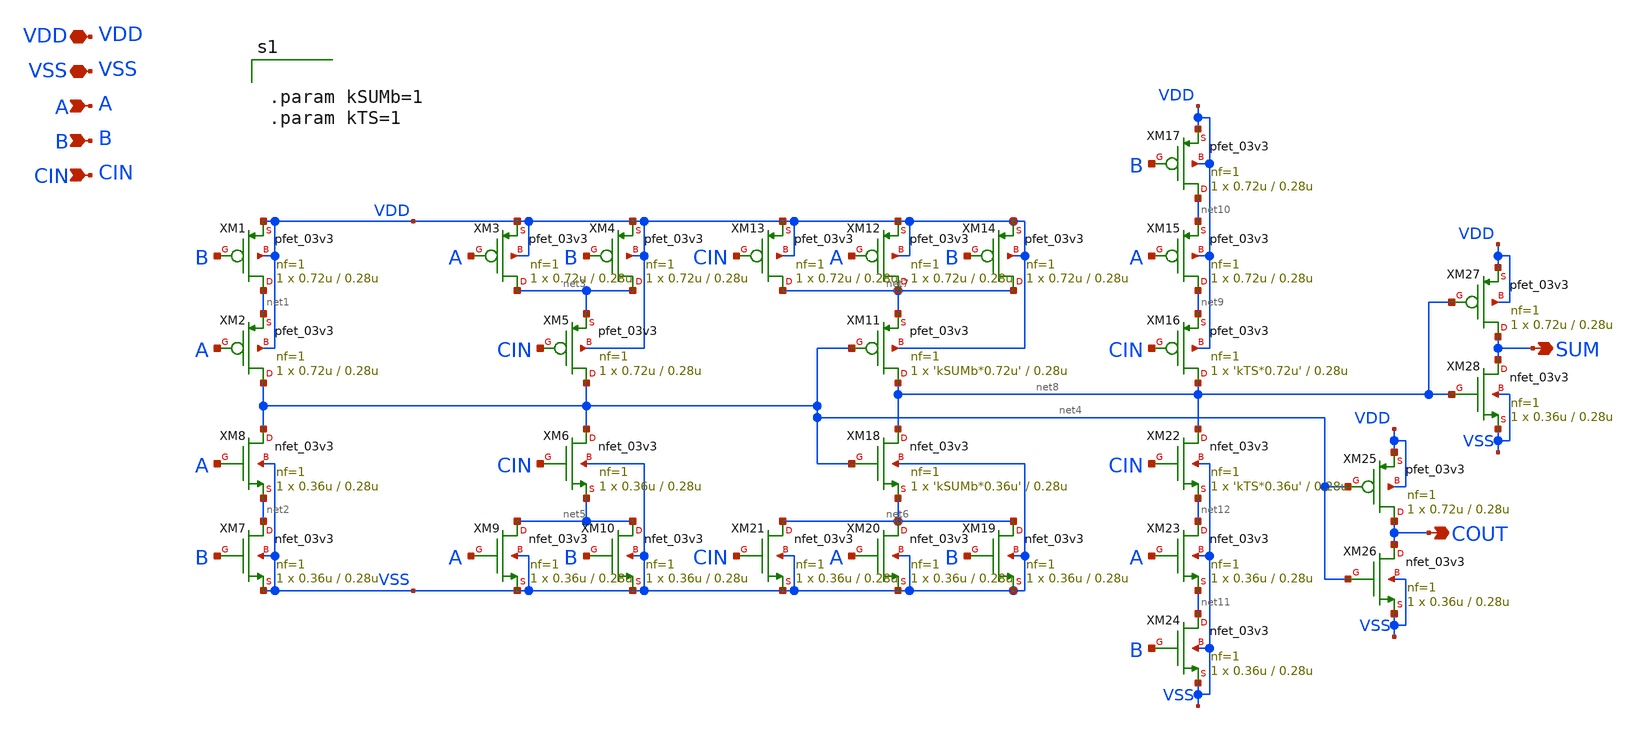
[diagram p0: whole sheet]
** sch_path: CAD6/pc_full_adder.sch
**.subckt pc_full_adder VDD VSS A B CIN COUT SUM
*.iopin VDD
*.iopin VSS
*.ipin A
*.ipin B
*.ipin CIN
*.opin COUT
*.opin SUM
XM1 net1 B VDD VDD pfet_03v3 L=0.28u W=0.72u nf=1 ad='int((nf+1)/2) * W/nf * 0.18u' as='int((nf+2)/2) * W/nf * 0.18u'
+ pd='2*int((nf+1)/2) * (W/nf + 0.18u)' ps='2*int((nf+2)/2) * (W/nf + 0.18u)' nrd='0.18u / W' nrs='0.18u / W'
+ sa=0 sb=0 sd=0 m=1
XM2 net4 A net1 VDD pfet_03v3 L=0.28u W=0.72u nf=1 ad='int((nf+1)/2) * W/nf * 0.18u' as='int((nf+2)/2) * W/nf * 0.18u'
+ pd='2*int((nf+1)/2) * (W/nf + 0.18u)' ps='2*int((nf+2)/2) * (W/nf + 0.18u)' nrd='0.18u / W' nrs='0.18u / W'
+ sa=0 sb=0 sd=0 m=1
XM3 net3 A VDD VDD pfet_03v3 L=0.28u W=0.72u nf=1 ad='int((nf+1)/2) * W/nf * 0.18u' as='int((nf+2)/2) * W/nf * 0.18u'
+ pd='2*int((nf+1)/2) * (W/nf + 0.18u)' ps='2*int((nf+2)/2) * (W/nf + 0.18u)' nrd='0.18u / W' nrs='0.18u / W'
+ sa=0 sb=0 sd=0 m=1
XM4 net3 B VDD VDD pfet_03v3 L=0.28u W=0.72u nf=1 ad='int((nf+1)/2) * W/nf * 0.18u' as='int((nf+2)/2) * W/nf * 0.18u'
+ pd='2*int((nf+1)/2) * (W/nf + 0.18u)' ps='2*int((nf+2)/2) * (W/nf + 0.18u)' nrd='0.18u / W' nrs='0.18u / W'
+ sa=0 sb=0 sd=0 m=1
XM5 net4 CIN net3 VDD pfet_03v3 L=0.28u W=0.72u nf=1 ad='int((nf+1)/2) * W/nf * 0.18u' as='int((nf+2)/2) * W/nf * 0.18u'
+ pd='2*int((nf+1)/2) * (W/nf + 0.18u)' ps='2*int((nf+2)/2) * (W/nf + 0.18u)' nrd='0.18u / W' nrs='0.18u / W'
+ sa=0 sb=0 sd=0 m=1
XM6 net4 CIN net5 VSS nfet_03v3 L=0.28u W=0.36u nf=1 ad='int((nf+1)/2) * W/nf * 0.18u' as='int((nf+2)/2) * W/nf * 0.18u'
+ pd='2*int((nf+1)/2) * (W/nf + 0.18u)' ps='2*int((nf+2)/2) * (W/nf + 0.18u)' nrd='0.18u / W' nrs='0.18u / W'
+ sa=0 sb=0 sd=0 m=1
XM7 net2 B VSS VSS nfet_03v3 L=0.28u W=0.36u nf=1 ad='int((nf+1)/2) * W/nf * 0.18u' as='int((nf+2)/2) * W/nf * 0.18u'
+ pd='2*int((nf+1)/2) * (W/nf + 0.18u)' ps='2*int((nf+2)/2) * (W/nf + 0.18u)' nrd='0.18u / W' nrs='0.18u / W'
+ sa=0 sb=0 sd=0 m=1
XM8 net4 A net2 VSS nfet_03v3 L=0.28u W=0.36u nf=1 ad='int((nf+1)/2) * W/nf * 0.18u' as='int((nf+2)/2) * W/nf * 0.18u'
+ pd='2*int((nf+1)/2) * (W/nf + 0.18u)' ps='2*int((nf+2)/2) * (W/nf + 0.18u)' nrd='0.18u / W' nrs='0.18u / W'
+ sa=0 sb=0 sd=0 m=1
XM9 net5 A VSS VSS nfet_03v3 L=0.28u W=0.36u nf=1 ad='int((nf+1)/2) * W/nf * 0.18u' as='int((nf+2)/2) * W/nf * 0.18u'
+ pd='2*int((nf+1)/2) * (W/nf + 0.18u)' ps='2*int((nf+2)/2) * (W/nf + 0.18u)' nrd='0.18u / W' nrs='0.18u / W'
+ sa=0 sb=0 sd=0 m=1
XM10 net5 B VSS VSS nfet_03v3 L=0.28u W=0.36u nf=1 ad='int((nf+1)/2) * W/nf * 0.18u' as='int((nf+2)/2) * W/nf * 0.18u'
+ pd='2*int((nf+1)/2) * (W/nf + 0.18u)' ps='2*int((nf+2)/2) * (W/nf + 0.18u)' nrd='0.18u / W' nrs='0.18u / W'
+ sa=0 sb=0 sd=0 m=1
XM11 net8 net4 net7 VDD pfet_03v3 L=0.28u W='kSUMb*0.72u' nf=1 ad='int((nf+1)/2) * W/nf * 0.18u' as='int((nf+2)/2) * W/nf * 0.18u'
+ pd='2*int((nf+1)/2) * (W/nf + 0.18u)' ps='2*int((nf+2)/2) * (W/nf + 0.18u)' nrd='0.18u / W' nrs='0.18u / W'
+ sa=0 sb=0 sd=0 m=1
XM12 net7 A VDD VDD pfet_03v3 L=0.28u W=0.72u nf=1 ad='int((nf+1)/2) * W/nf * 0.18u' as='int((nf+2)/2) * W/nf * 0.18u'
+ pd='2*int((nf+1)/2) * (W/nf + 0.18u)' ps='2*int((nf+2)/2) * (W/nf + 0.18u)' nrd='0.18u / W' nrs='0.18u / W'
+ sa=0 sb=0 sd=0 m=1
XM13 net7 CIN VDD VDD pfet_03v3 L=0.28u W=0.72u nf=1 ad='int((nf+1)/2) * W/nf * 0.18u' as='int((nf+2)/2) * W/nf * 0.18u'
+ pd='2*int((nf+1)/2) * (W/nf + 0.18u)' ps='2*int((nf+2)/2) * (W/nf + 0.18u)' nrd='0.18u / W' nrs='0.18u / W'
+ sa=0 sb=0 sd=0 m=1
XM14 net7 B VDD VDD pfet_03v3 L=0.28u W=0.72u nf=1 ad='int((nf+1)/2) * W/nf * 0.18u' as='int((nf+2)/2) * W/nf * 0.18u'
+ pd='2*int((nf+1)/2) * (W/nf + 0.18u)' ps='2*int((nf+2)/2) * (W/nf + 0.18u)' nrd='0.18u / W' nrs='0.18u / W'
+ sa=0 sb=0 sd=0 m=1
XM15 net9 A net10 VDD pfet_03v3 L=0.28u W=0.72u nf=1 ad='int((nf+1)/2) * W/nf * 0.18u' as='int((nf+2)/2) * W/nf * 0.18u'
+ pd='2*int((nf+1)/2) * (W/nf + 0.18u)' ps='2*int((nf+2)/2) * (W/nf + 0.18u)' nrd='0.18u / W' nrs='0.18u / W'
+ sa=0 sb=0 sd=0 m=1
XM16 net8 CIN net9 VDD pfet_03v3 L=0.28u W='kTS*0.72u' nf=1 ad='int((nf+1)/2) * W/nf * 0.18u' as='int((nf+2)/2) * W/nf * 0.18u'
+ pd='2*int((nf+1)/2) * (W/nf + 0.18u)' ps='2*int((nf+2)/2) * (W/nf + 0.18u)' nrd='0.18u / W' nrs='0.18u / W'
+ sa=0 sb=0 sd=0 m=1
XM17 net10 B VDD VDD pfet_03v3 L=0.28u W=0.72u nf=1 ad='int((nf+1)/2) * W/nf * 0.18u' as='int((nf+2)/2) * W/nf * 0.18u'
+ pd='2*int((nf+1)/2) * (W/nf + 0.18u)' ps='2*int((nf+2)/2) * (W/nf + 0.18u)' nrd='0.18u / W' nrs='0.18u / W'
+ sa=0 sb=0 sd=0 m=1
XM18 net8 net4 net6 VSS nfet_03v3 L=0.28u W='kSUMb*0.36u' nf=1 ad='int((nf+1)/2) * W/nf * 0.18u' as='int((nf+2)/2) * W/nf * 0.18u'
+ pd='2*int((nf+1)/2) * (W/nf + 0.18u)' ps='2*int((nf+2)/2) * (W/nf + 0.18u)' nrd='0.18u / W' nrs='0.18u / W'
+ sa=0 sb=0 sd=0 m=1
XM19 net6 B VSS VSS nfet_03v3 L=0.28u W=0.36u nf=1 ad='int((nf+1)/2) * W/nf * 0.18u' as='int((nf+2)/2) * W/nf * 0.18u'
+ pd='2*int((nf+1)/2) * (W/nf + 0.18u)' ps='2*int((nf+2)/2) * (W/nf + 0.18u)' nrd='0.18u / W' nrs='0.18u / W'
+ sa=0 sb=0 sd=0 m=1
XM20 net6 A VSS VSS nfet_03v3 L=0.28u W=0.36u nf=1 ad='int((nf+1)/2) * W/nf * 0.18u' as='int((nf+2)/2) * W/nf * 0.18u'
+ pd='2*int((nf+1)/2) * (W/nf + 0.18u)' ps='2*int((nf+2)/2) * (W/nf + 0.18u)' nrd='0.18u / W' nrs='0.18u / W'
+ sa=0 sb=0 sd=0 m=1
XM21 net6 CIN VSS VSS nfet_03v3 L=0.28u W=0.36u nf=1 ad='int((nf+1)/2) * W/nf * 0.18u' as='int((nf+2)/2) * W/nf * 0.18u'
+ pd='2*int((nf+1)/2) * (W/nf + 0.18u)' ps='2*int((nf+2)/2) * (W/nf + 0.18u)' nrd='0.18u / W' nrs='0.18u / W'
+ sa=0 sb=0 sd=0 m=1
XM22 net8 CIN net12 VSS nfet_03v3 L=0.28u W='kTS*0.36u' nf=1 ad='int((nf+1)/2) * W/nf * 0.18u' as='int((nf+2)/2) * W/nf * 0.18u'
+ pd='2*int((nf+1)/2) * (W/nf + 0.18u)' ps='2*int((nf+2)/2) * (W/nf + 0.18u)' nrd='0.18u / W' nrs='0.18u / W'
+ sa=0 sb=0 sd=0 m=1
XM23 net12 A net11 VSS nfet_03v3 L=0.28u W=0.36u nf=1 ad='int((nf+1)/2) * W/nf * 0.18u' as='int((nf+2)/2) * W/nf * 0.18u'
+ pd='2*int((nf+1)/2) * (W/nf + 0.18u)' ps='2*int((nf+2)/2) * (W/nf + 0.18u)' nrd='0.18u / W' nrs='0.18u / W'
+ sa=0 sb=0 sd=0 m=1
XM24 net11 B VSS VSS nfet_03v3 L=0.28u W=0.36u nf=1 ad='int((nf+1)/2) * W/nf * 0.18u' as='int((nf+2)/2) * W/nf * 0.18u'
+ pd='2*int((nf+1)/2) * (W/nf + 0.18u)' ps='2*int((nf+2)/2) * (W/nf + 0.18u)' nrd='0.18u / W' nrs='0.18u / W'
+ sa=0 sb=0 sd=0 m=1
XM25 COUT net4 VDD VDD pfet_03v3 L=0.28u W=0.72u nf=1 ad='int((nf+1)/2) * W/nf * 0.18u' as='int((nf+2)/2) * W/nf * 0.18u'
+ pd='2*int((nf+1)/2) * (W/nf + 0.18u)' ps='2*int((nf+2)/2) * (W/nf + 0.18u)' nrd='0.18u / W' nrs='0.18u / W'
+ sa=0 sb=0 sd=0 m=1
XM26 COUT net4 VSS VSS nfet_03v3 L=0.28u W=0.36u nf=1 ad='int((nf+1)/2) * W/nf * 0.18u' as='int((nf+2)/2) * W/nf * 0.18u'
+ pd='2*int((nf+1)/2) * (W/nf + 0.18u)' ps='2*int((nf+2)/2) * (W/nf + 0.18u)' nrd='0.18u / W' nrs='0.18u / W'
+ sa=0 sb=0 sd=0 m=1
XM27 SUM net8 VDD VDD pfet_03v3 L=0.28u W=0.72u nf=1 ad='int((nf+1)/2) * W/nf * 0.18u' as='int((nf+2)/2) * W/nf * 0.18u'
+ pd='2*int((nf+1)/2) * (W/nf + 0.18u)' ps='2*int((nf+2)/2) * (W/nf + 0.18u)' nrd='0.18u / W' nrs='0.18u / W'
+ sa=0 sb=0 sd=0 m=1
XM28 SUM net8 VSS VSS nfet_03v3 L=0.28u W=0.36u nf=1 ad='int((nf+1)/2) * W/nf * 0.18u' as='int((nf+2)/2) * W/nf * 0.18u'
+ pd='2*int((nf+1)/2) * (W/nf + 0.18u)' ps='2*int((nf+2)/2) * (W/nf + 0.18u)' nrd='0.18u / W' nrs='0.18u / W'
+ sa=0 sb=0 sd=0 m=1
**** begin user architecture code


.param kSUMb=1
.param kTS=1


**** end user architecture code
**.ends
.end
